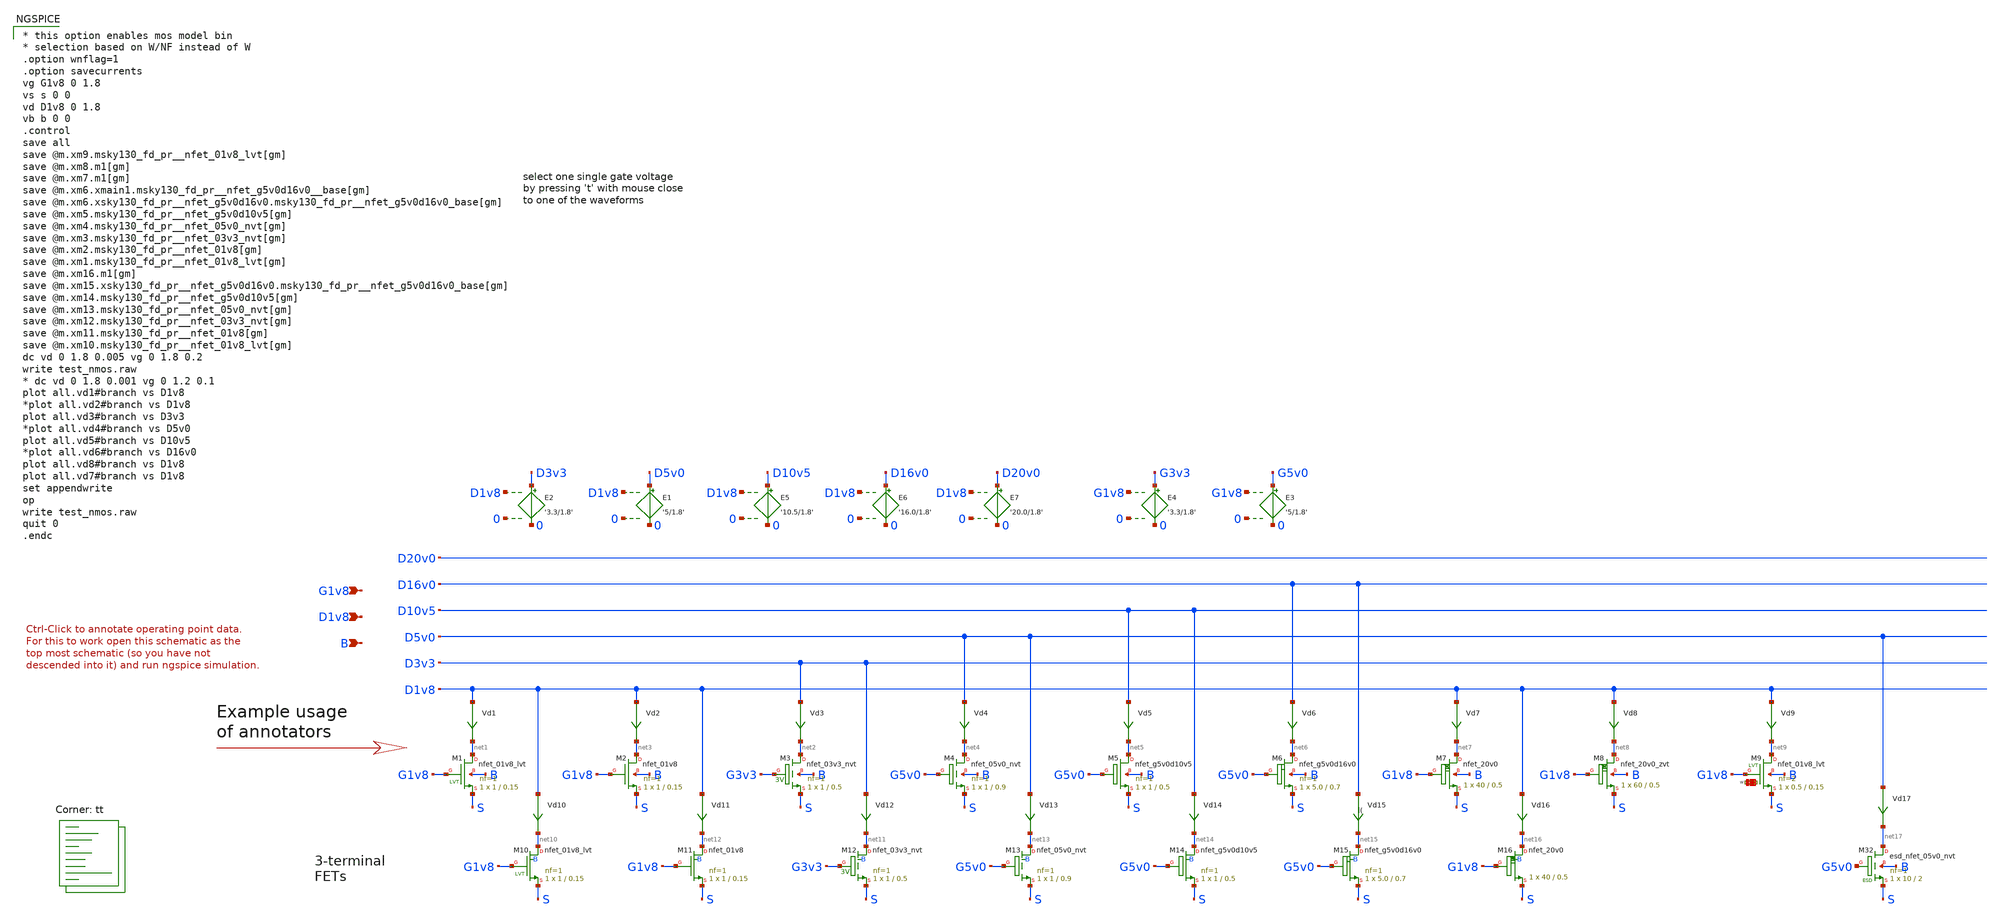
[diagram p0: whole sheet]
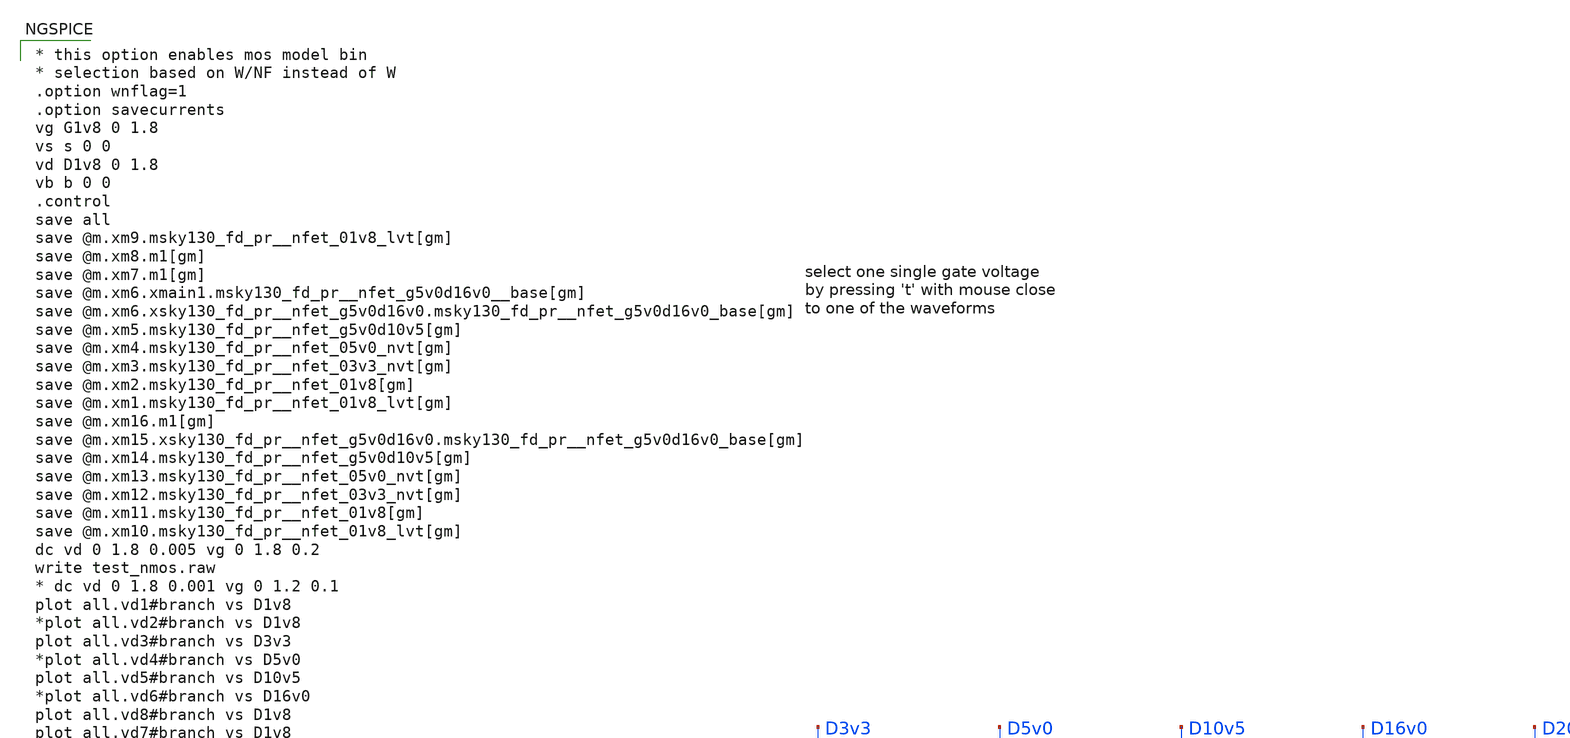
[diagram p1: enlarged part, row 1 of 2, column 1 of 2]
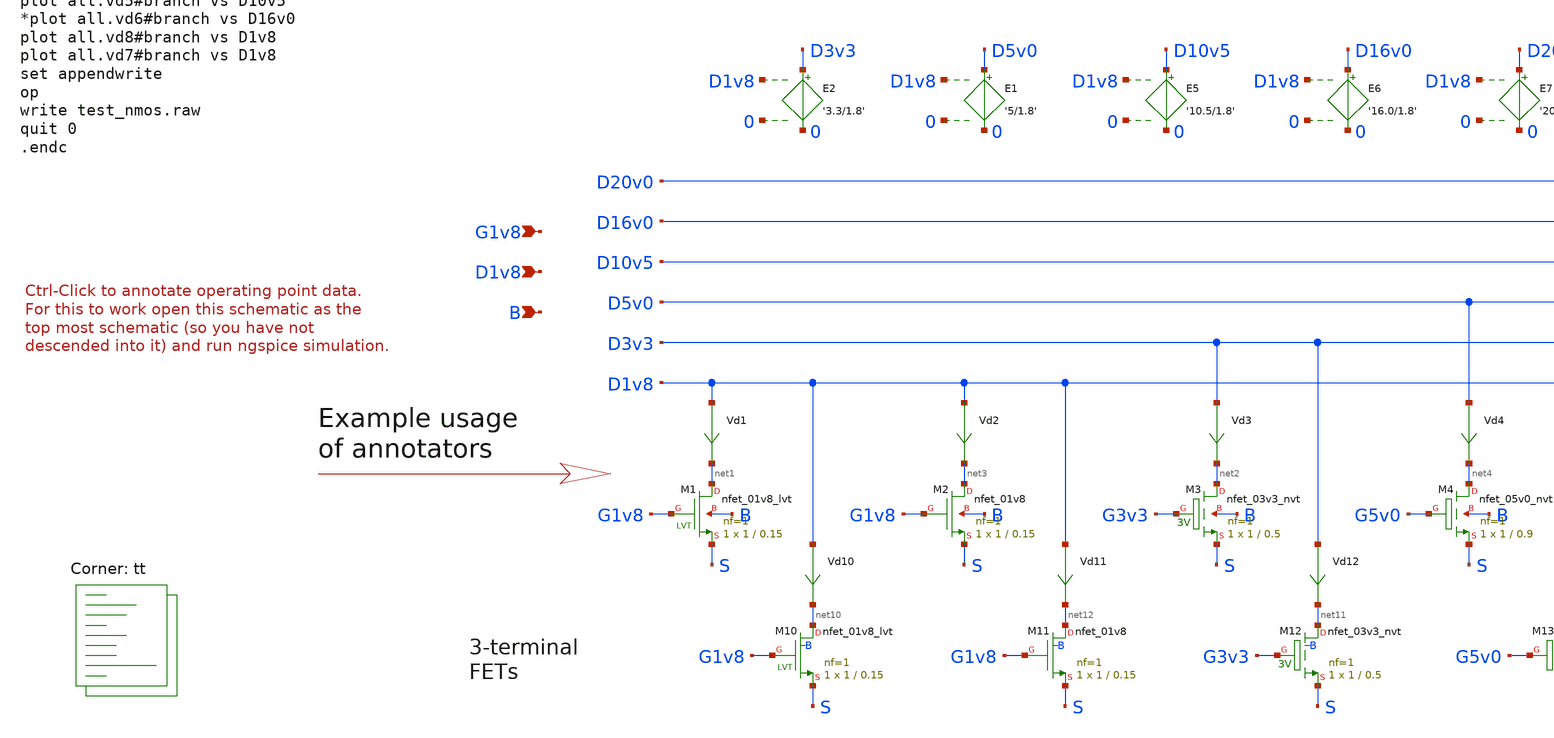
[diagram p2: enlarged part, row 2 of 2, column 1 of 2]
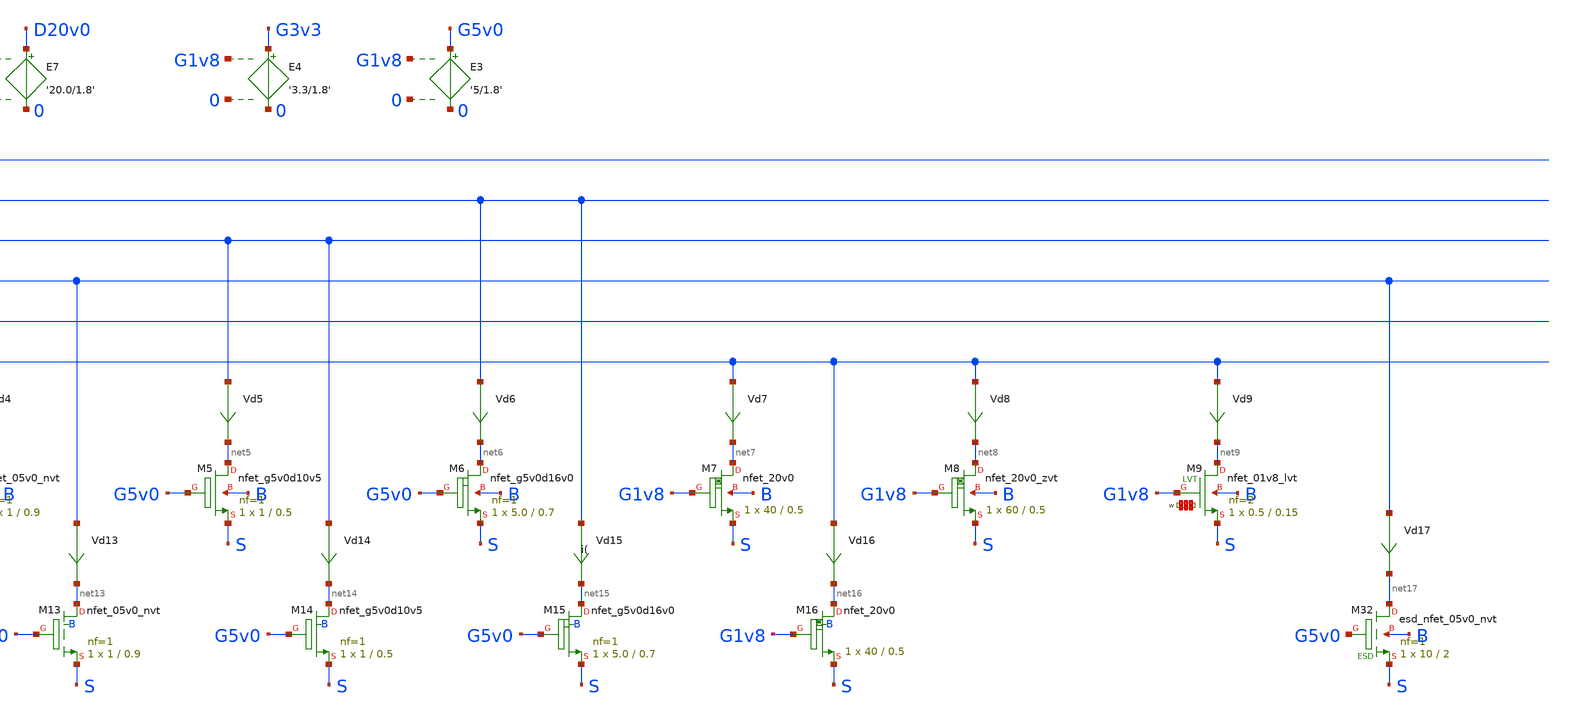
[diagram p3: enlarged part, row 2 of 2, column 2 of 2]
** sch_path: sky130A/xschem_libs/sky130_tests/test_nmos/schematic/test_nmos.sch
* Copyright 2021 Stefan Frederik Schippers
* Licensed under the Apache License, Version 2.0 (the "License");
* you may not use this file except in compliance with the License.
* You may obtain a copy of the License at
* https://www.apache.org/licenses/LICENSE-2.0
* Unless required by applicable law or agreed to in writing, software
* distributed under the License is distributed on an "AS IS" BASIS,
* WITHOUT WARRANTIES OR CONDITIONS OF ANY KIND, either express or implied.
* See the License for the specific language governing permissions and
* limitations under the License.
**.subckt test_nmos G1v8 D1v8 B
*.ipin G1v8
*.ipin D1v8
*.ipin B
Vd1 D1v8 net1 0
.save i(vd1)
Vd3 D3v3 net2 0
.save i(vd3)
Vd2 D1v8 net3 0
.save i(vd2)
Vd4 D5v0 net4 0
.save i(vd4)
E1 D5v0 0 D1v8 0 '5/1.8'
E2 D3v3 0 D1v8 0 '3.3/1.8'
E3 G5v0 0 G1v8 0 '5/1.8'
E4 G3v3 0 G1v8 0 '3.3/1.8'
Vd5 D10v5 net5 0
.save i(vd5)
E5 D10v5 0 D1v8 0 '10.5/1.8'
E6 D16v0 0 D1v8 0 '16.0/1.8'
Vd6 D16v0 net6 0
.save i(vd6)
Vd7 D1v8 net7 0
.save i(vd7)
E7 D20v0 0 D1v8 0 '20.0/1.8'
XM1 net1 G1v8 S B sky130_fd_pr__nfet_01v8_lvt L=0.15 W=1 nf=1 ad='int((1 + 1)/2) * 1 / 1 * 0.29' as='int((1 + 2)/2) * 1 / 1 * 0.29'
+ pd='2*int((1 + 1)/2) * (1 / 1 + 0.29)' ps='2*int((1 + 2)/2) * (1 / 1 + 0.29)' nrd='0.29 / 1 ' nrs='0.29 / 1 '
+ sa=0 sb=0 sd=0 mult=1 m=1
XM2 net3 G1v8 S B sky130_fd_pr__nfet_01v8 L=0.15 W=1 nf=1 ad='int((1 + 1)/2) * 1 / 1 * 0.29' as='int((1 + 2)/2) * 1 / 1 * 0.29'
+ pd='2*int((1 + 1)/2) * (1 / 1 + 0.29)' ps='2*int((1 + 2)/2) * (1 / 1 + 0.29)' nrd='0.29 / 1 ' nrs='0.29 / 1 '
+ sa=0 sb=0 sd=0 mult=1 m=1
XM3 net2 G3v3 S B sky130_fd_pr__nfet_03v3_nvt L=0.5 W=1 nf=1 ad='int((1 + 1)/2) * 1 / 1 * 0.29' as='int((1 + 2)/2) * 1 / 1 * 0.29'
+ pd='2*int((1 + 1)/2) * (1 / 1 + 0.29)' ps='2*int((1 + 2)/2) * (1 / 1 + 0.29)' nrd='0.29 / 1 ' nrs='0.29 / 1 '
+ sa=0 sb=0 sd=0 mult=1 m=1
XM4 net4 G5v0 S B sky130_fd_pr__nfet_05v0_nvt L=0.9 W=1 nf=1 ad='int((1 + 1)/2) * 1 / 1 * 0.29' as='int((1 + 2)/2) * 1 / 1 * 0.29'
+ pd='2*int((1 + 1)/2) * (1 / 1 + 0.29)' ps='2*int((1 + 2)/2) * (1 / 1 + 0.29)' nrd='0.29 / 1 ' nrs='0.29 / 1 '
+ sa=0 sb=0 sd=0 mult=1 m=1
XM5 net5 G5v0 S B sky130_fd_pr__nfet_g5v0d10v5 L=0.5 W=1 nf=1 ad='int((1 + 1)/2) * 1 / 1 * 0.29' as='int((1 + 2)/2) * 1 / 1 * 0.29'
+ pd='2*int((1 + 1)/2) * (1 / 1 + 0.29)' ps='2*int((1 + 2)/2) * (1 / 1 + 0.29)' nrd='0.29 / 1 ' nrs='0.29 / 1 '
+ sa=0 sb=0 sd=0 mult=1 m=1
XM6 net6 G5v0 S B sky130_fd_pr__nfet_g5v0d16v0 L=0.7 W=5.0 nf=1 ad='int((nf+1)/2) * W/nf * 0.29' as='int((nf+2)/2) * W/nf * 0.29'
+ pd='2*int((nf+1)/2) * (W/nf + 0.29)' ps='2*int((nf+2)/2) * (W/nf + 0.29)' nrd='0.29 / W' nrs='0.29 / W'
+ sa=0 sb=0 sd=0 mult=1 m=1
Vd8 D1v8 net8 0
.save i(vd8)
XM7 net7 G1v8 S B sky130_fd_pr__nfet_20v0 L=0.5 W=40 m=1
XM8 net8 G1v8 S B sky130_fd_pr__nfet_20v0_zvt W=60 L=0.5 m=1
Vd9 D1v8 net9 0
.save i(vd9)
XM9 net9 G1v8 S B sky130_fd_pr__nfet_01v8_lvt L=0.15 W='0.5 * 2 ' nf=2 ad='int((2 + 1)/2) * 0.5 / 2 * 0.29'
+ as='int((2 + 2)/2) * 0.5 / 2 * 0.29' pd='2*int((2 + 1)/2) * (0.5 / 2 + 0.29)' ps='2*int((2 + 2)/2) * (0.5 / 2 + 0.29)'
+ nrd='0.29 / 0.5 ' nrs='0.29 / 0.5 ' sa=0 sb=0 sd=0 mult=1 m=1
Vd10 D1v8 net10 0
.save i(vd10)
Vd11 D1v8 net12 0
.save i(vd11)
Vd12 D3v3 net11 0
.save i(vd12)
Vd13 D5v0 net13 0
.save i(vd13)
Vd14 D10v5 net14 0
.save i(vd14)
Vd15 D16v0 net15 0
.save i(vd15)
Vd16 D1v8 net16 0
.save i(vd16)
XM10 net10 G1v8 S B sky130_fd_pr__nfet_01v8_lvt L=0.15 W=1 nf=1 ad='int((1 + 1)/2) * 1 / 1 * 0.29' as='int((1 + 2)/2) * 1 / 1 * 0.29'
+ pd='2*int((1 + 1)/2) * (1 / 1 + 0.29)' ps='2*int((1 + 2)/2) * (1 / 1 + 0.29)' nrd='0.29 / 1 ' nrs='0.29 / 1 '
+ sa=0 sb=0 sd=0 mult=1 m=1
XM11 net12 G1v8 S B sky130_fd_pr__nfet_01v8 L=0.15 W=1 nf=1 ad='int((nf+1)/2) * W/nf * 0.29' as='int((nf+2)/2) * W/nf * 0.29'
+ pd='2*int((nf+1)/2) * (W/nf + 0.29)' ps='2*int((nf+2)/2) * (W/nf + 0.29)' nrd='0.29 / W' nrs='0.29 / W'
+ sa=0 sb=0 sd=0 mult=1 m=1
XM12 net11 G3v3 S B sky130_fd_pr__nfet_03v3_nvt L=0.5 W=1 nf=1 ad='int((1 + 1)/2) * 1 / 1 * 0.29' as='int((1 + 2)/2) * 1 / 1 * 0.29'
+ pd='2*int((1 + 1)/2) * (1 / 1 + 0.29)' ps='2*int((1 + 2)/2) * (1 / 1 + 0.29)' nrd='0.29 / 1 ' nrs='0.29 / 1 '
+ sa=0 sb=0 sd=0 mult=1 m=1
XM13 net13 G5v0 S B sky130_fd_pr__nfet_05v0_nvt L=0.9 W=1 nf=1 ad='int((1 + 1)/2) * 1 / 1 * 0.29' as='int((1 + 2)/2) * 1 / 1 * 0.29'
+ pd='2*int((1 + 1)/2) * (1 / 1 + 0.29)' ps='2*int((1 + 2)/2) * (1 / 1 + 0.29)' nrd='0.29 / 1 ' nrs='0.29 / 1 '
+ sa=0 sb=0 sd=0 mult=1 m=1
XM14 net14 G5v0 S B sky130_fd_pr__nfet_g5v0d10v5 L=0.5 W=1 nf=1 ad='int((nf+1)/2) * W/nf * 0.29' as='int((nf+2)/2) * W/nf * 0.29'
+ pd='2*int((nf+1)/2) * (W/nf + 0.29)' ps='2*int((nf+2)/2) * (W/nf + 0.29)' nrd='0.29 / W' nrs='0.29 / W'
+ sa=0 sb=0 sd=0 mult=1 m=1
XM15 net15 G5v0 S B sky130_fd_pr__nfet_g5v0d16v0 L=0.7 W=5.0 nf=1 ad='int((nf+1)/2) * W/nf * 0.29' as='int((nf+2)/2) * W/nf * 0.29'
+ pd='2*int((nf+1)/2) * (W/nf + 0.29)' ps='2*int((nf+2)/2) * (W/nf + 0.29)' nrd='0.29 / W' nrs='0.29 / W'
+ sa=0 sb=0 sd=0 mult=1 m=1
XM16 net16 G1v8 S B sky130_fd_pr__nfet_20v0 L=0.5 W=40 m=1
XM32 net17 G5v0 S B sky130_fd_pr__esd_nfet_05v0_nvt L=2 W=10 nf=1 ad='int((1 + 1)/2) * 10 / 1 * 0.29'
+ as='int((1 + 2)/2) * 10 / 1 * 0.29' pd='2*int((1 + 1)/2) * (10 / 1 + 0.29)' ps='2*int((1 + 2)/2) * (10 / 1 + 0.29)'
+ nrd='0.29 / 10 ' nrs='0.29 / 10 ' sa=0 sb=0 sd=0 mult=1 m=1
Vd17 D5v0 net17 0
.save i(vd17)
**** begin user architecture code

* this option enables mos model bin
* selection based on W/NF instead of W
.option wnflag=1
.option savecurrents
vg G1v8 0 1.8
vs s 0 0
vd D1v8 0 1.8
vb b 0 0
.control
save all
save @m.xm9.msky130_fd_pr__nfet_01v8_lvt[gm]
save @m.xm8.m1[gm]
save @m.xm7.m1[gm]
save @m.xm6.xmain1.msky130_fd_pr__nfet_g5v0d16v0__base[gm]
save @m.xm6.xsky130_fd_pr__nfet_g5v0d16v0.msky130_fd_pr__nfet_g5v0d16v0_base[gm]
save @m.xm5.msky130_fd_pr__nfet_g5v0d10v5[gm]
save @m.xm4.msky130_fd_pr__nfet_05v0_nvt[gm]
save @m.xm3.msky130_fd_pr__nfet_03v3_nvt[gm]
save @m.xm2.msky130_fd_pr__nfet_01v8[gm]
save @m.xm1.msky130_fd_pr__nfet_01v8_lvt[gm]
save @m.xm16.m1[gm]
save @m.xm15.xsky130_fd_pr__nfet_g5v0d16v0.msky130_fd_pr__nfet_g5v0d16v0_base[gm]
save @m.xm14.msky130_fd_pr__nfet_g5v0d10v5[gm]
save @m.xm13.msky130_fd_pr__nfet_05v0_nvt[gm]
save @m.xm12.msky130_fd_pr__nfet_03v3_nvt[gm]
save @m.xm11.msky130_fd_pr__nfet_01v8[gm]
save @m.xm10.msky130_fd_pr__nfet_01v8_lvt[gm]
dc vd 0 1.8 0.005 vg 0 1.8 0.2
write test_nmos.raw
* dc vd 0 1.8 0.001 vg 0 1.2 0.1
plot all.vd1#branch vs D1v8
*plot all.vd2#branch vs D1v8
plot all.vd3#branch vs D3v3
*plot all.vd4#branch vs D5v0
plot all.vd5#branch vs D10v5
*plot all.vd6#branch vs D16v0
plot all.vd8#branch vs D1v8
plot all.vd7#branch vs D1v8
set appendwrite
op
write test_nmos.raw
quit 0
.endc


.lib $::SKYWATER_MODELS/sky130.lib.spice tt
**** end user architecture code
**.ends
.end
